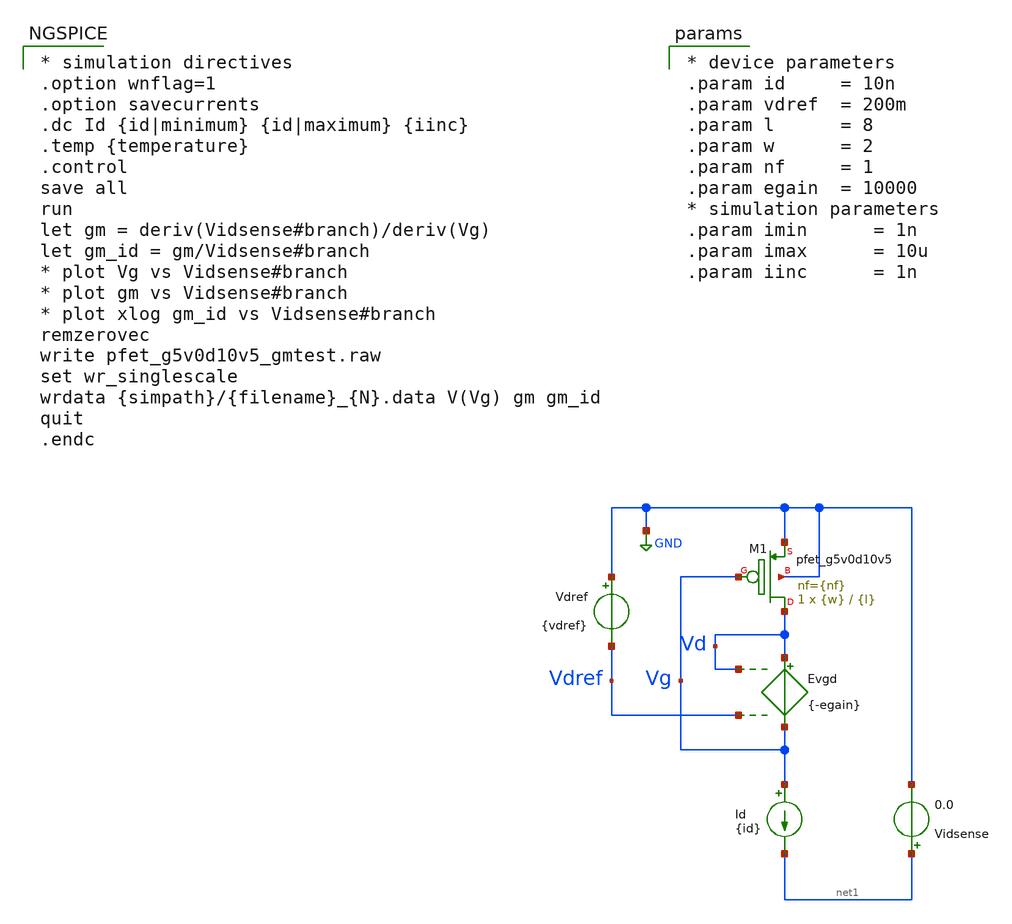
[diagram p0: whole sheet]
** sch_path: cace/tb_pfet_g5v0d10v5_gmtest.sch
**.subckt tb_pfet_g5v0d10v5_gmtest
Evgd Vd Vg Vd Vdref {-egain}
Id Vg net1 {id}
Vdref GND Vdref {vdref}
Vidsense net1 GND 0.0
XM1 Vd Vg GND GND sky130_fd_pr__pfet_g5v0d10v5 L={l} W={w} nf={nf} ad='int(({nf} + 1)/2) * {w} / {nf} * 0.29'
+ as='int(({nf} + 2)/2) * {w} / {nf} * 0.29' pd='2*int(({nf} + 1)/2) * ({w} / {nf} + 0.29)' ps='2*int(({nf} + 2)/2) * ({w} / {nf} + 0.29)'
+ nrd='0.29 / {w} ' nrs='0.29 / {w} ' sa=0 sb=0 sd=0 mult=1 m=1
**** begin user architecture code

** opencircuitdesign pdks install
.lib $::SKYWATER_MODELS/sky130.lib.spice {corner}



* simulation directives
.option wnflag=1
.option savecurrents
.dc Id {id|minimum} {id|maximum} {iinc}
.temp {temperature}
.control
save all
run
let gm = deriv(Vidsense#branch)/deriv(Vg)
let gm_id = gm/Vidsense#branch
* plot Vg vs Vidsense#branch
* plot gm vs Vidsense#branch
* plot xlog gm_id vs Vidsense#branch
remzerovec
write pfet_g5v0d10v5_gmtest.raw
set wr_singlescale
wrdata {simpath}/{filename}_{N}.data V(Vg) gm gm_id
quit
.endc



* device parameters
.param id     = 10n
.param vdref  = 200m
.param l      = 8
.param w      = 2
.param nf     = 1
.param egain  = 10000
* simulation parameters
.param imin      = 1n
.param imax      = 10u
.param iinc      = 1n


**** end user architecture code
**.ends
.GLOBAL GND
.end
